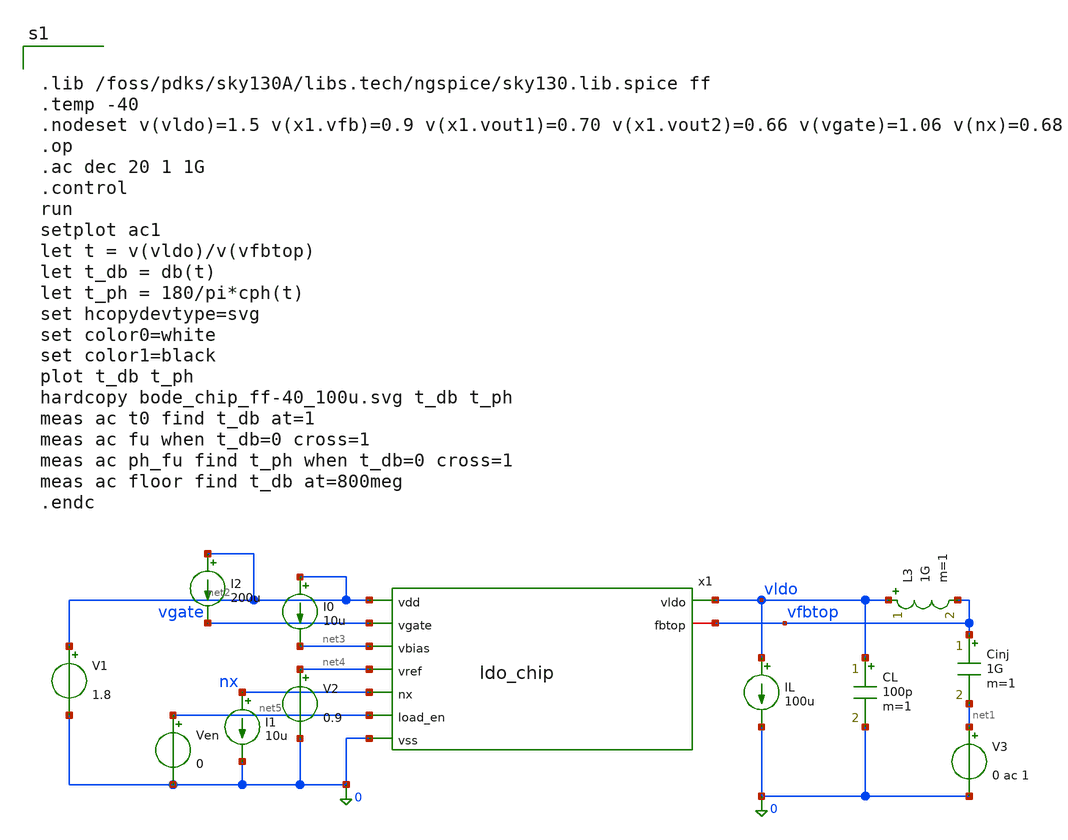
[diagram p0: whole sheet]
** sch_path: ldo_top.sch
**.subckt ldo_top
L3 vldo vfbtop 1G m=1
Cinj vfbtop net1 1G m=1
V3 net1 0 0 ac 1
I0 net2 net3 10u
V1 net2 0 1.8
V2 net4 0 0.9
I1 nx 0 10u
I2 net2 vgate 200u
Ven net5 0 0
CL vldo 0 100p m=1
IL vldo 0 100u
x1 net2 vgate net3 net4 vldo vfbtop nx net5 0 ldo_chip
**** begin user architecture code


.lib /foss/pdks/sky130A/libs.tech/ngspice/sky130.lib.spice ff
.temp -40
.nodeset v(vldo)=1.5 v(x1.vfb)=0.9 v(x1.vout1)=0.70 v(x1.vout2)=0.66 v(vgate)=1.06 v(nx)=0.68
.op
.ac dec 20 1 1G
.control
run
setplot ac1
let t = v(vldo)/v(vfbtop)
let t_db = db(t)
let t_ph = 180/pi*cph(t)
set hcopydevtype=svg
set color0=white
set color1=black
plot t_db t_ph
hardcopy bode_chip_ff-40_100u.svg t_db t_ph
meas ac t0 find t_db at=1
meas ac fu when t_db=0 cross=1
meas ac ph_fu find t_ph when t_db=0 cross=1
meas ac floor find t_db at=800meg
.endc


**** end user architecture code
**.ends
.end
